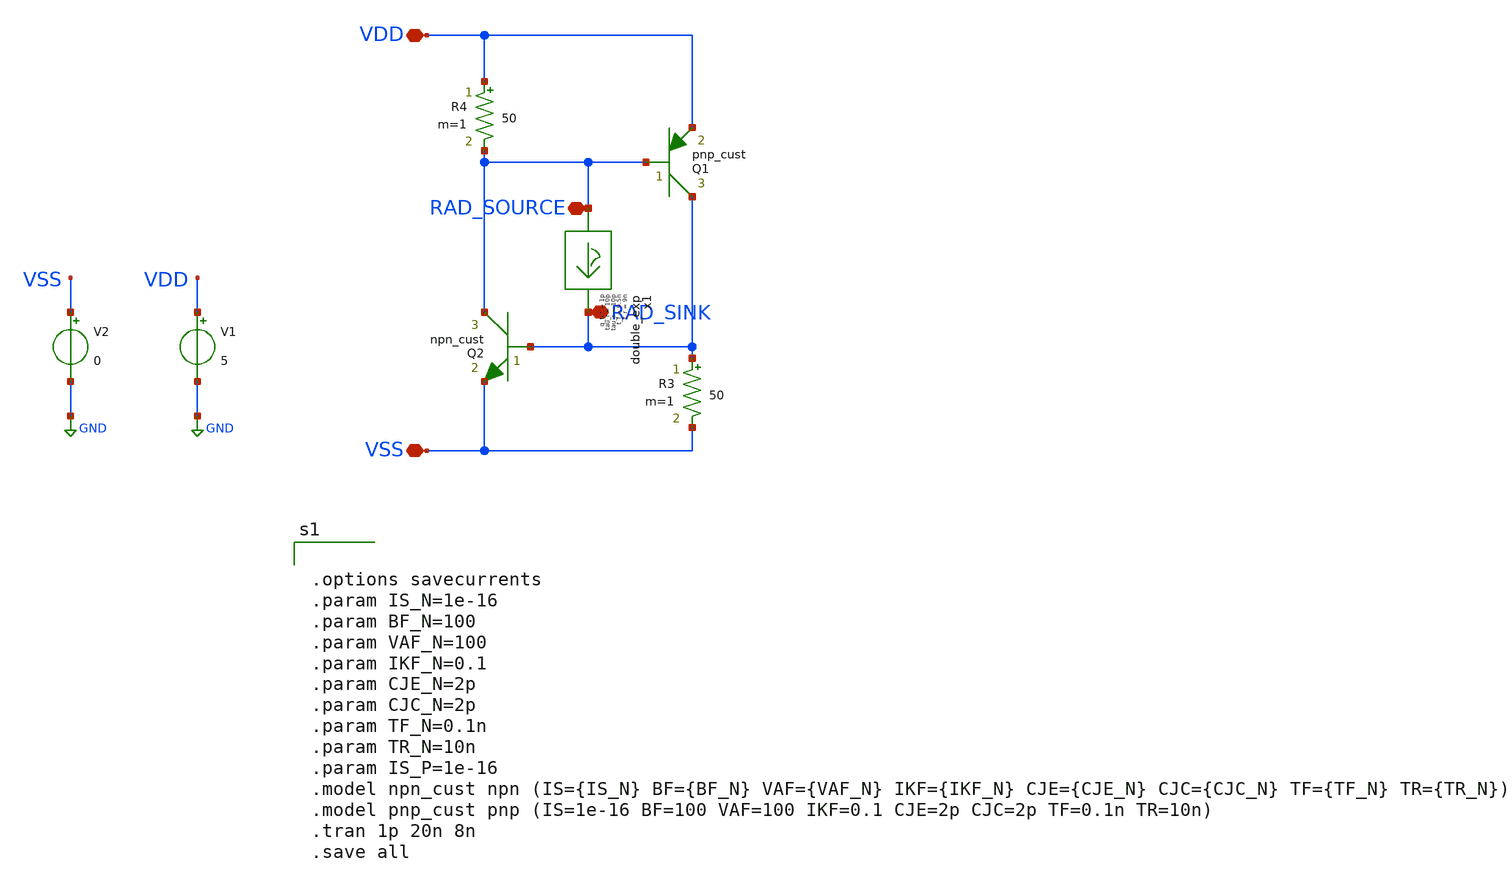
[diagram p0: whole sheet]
** sch_path: latchup/basic.sch
**.subckt basic VDD VSS RAD_SOURCE RAD_SINK
*.iopin VDD
*.iopin VSS
*.iopin RAD_SOURCE
*.iopin RAD_SINK
Q1 RAD_SINK RAD_SOURCE VDD pnp_cust area=1 m=1
Q2 RAD_SOURCE RAD_SINK VSS npn_cust area=1 m=1
R3 RAD_SINK VSS 50 m=1
R4 VDD RAD_SOURCE 50 m=1
V1 VDD GND 5
x1 RAD_SOURCE RAD_SINK double_exp t_r=9n tau_r=10p t_f=9.5n tau_f=10p q_tot=1p
V2 VSS GND 0
**** begin user architecture code


.options savecurrents
.param IS_N=1e-16
.param BF_N=100
.param VAF_N=100
.param IKF_N=0.1
.param CJE_N=2p
.param CJC_N=2p
.param TF_N=0.1n
.param TR_N=10n
.param IS_P=1e-16
.model npn_cust npn (IS={IS_N} BF={BF_N} VAF={VAF_N} IKF={IKF_N} CJE={CJE_N} CJC={CJC_N} TF={TF_N} TR={TR_N})
.model pnp_cust pnp (IS=1e-16 BF=100 VAF=100 IKF=0.1 CJE=2p CJC=2p TF=0.1n TR=10n)
.tran 1p 20n 8n
.save all




.include /usr/local/share/rad_modeling_blocks/rad_modeling_blocks.spice


**** end user architecture code
**.ends

* expanding   symbol:  double_exp.sym # of pins=2
** sym_path: xschem_rad_library/double_exp.sym
** sch_path: xschem_rad_library/double_exp.sch
.subckt double_exp in out  t_r=0 t_f=0 tau_r=0 tau_f=0 q_tot=0
*.opin OUT
*.ipin IN
I1 IN OUT EXP(0 {q_tot / (t_f-t_r+tau_f-tau_r)} {t_r} {tau_r} {t_f} {tau_f})
.ends

.GLOBAL GND
.end
